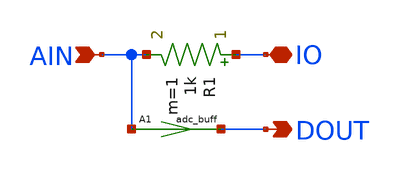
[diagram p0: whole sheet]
** sch_path: xschem_library/devices/vams_mixed_io.sch
**.subckt vams_mixed_io IO AIN DOUT
*.iopin IO
*.ipin AIN
*.opin DOUT
R1 IO AIN 1k m=1
A1 [ AIN ] [ DOUT ] adc_buff
**.ends
.end
